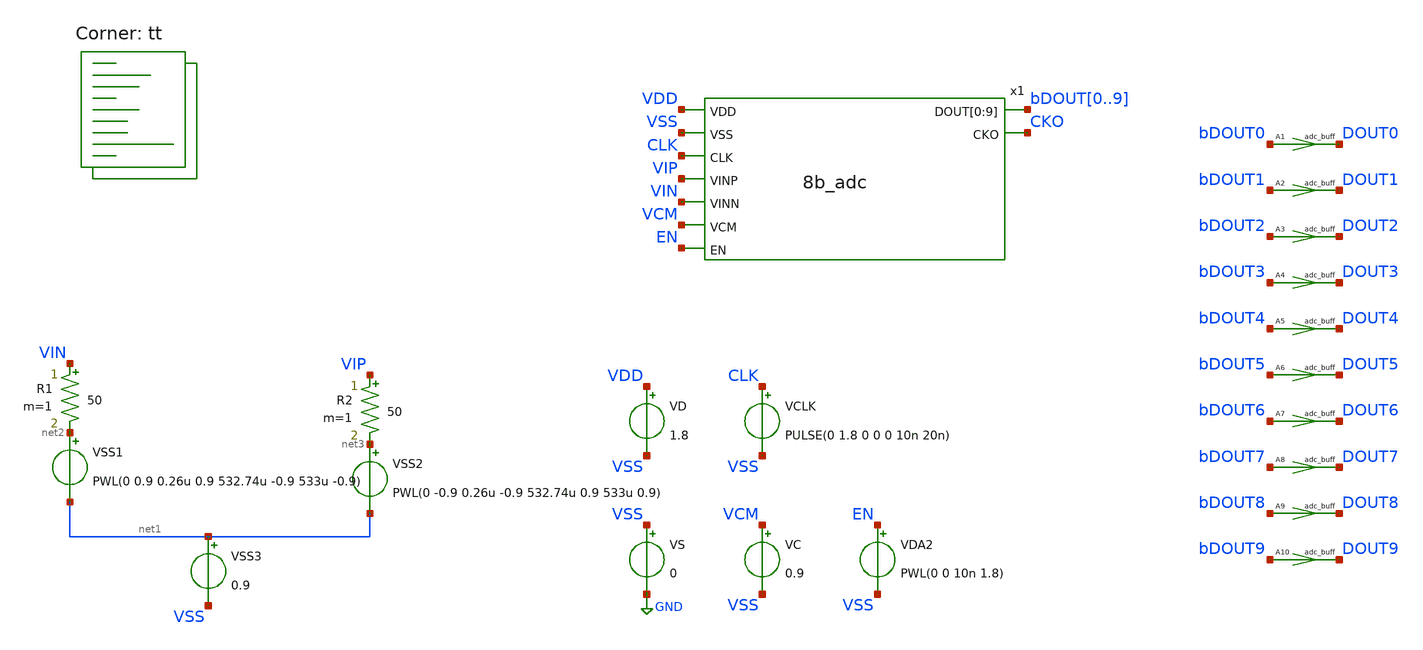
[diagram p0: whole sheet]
** sch_path: xschem/adc_tb_static.sch
**.subckt adc_tb_static
VSS1 net2 net1 PWL(0 0.9 0.26u 0.9 532.74u -0.9 533u -0.9)
VSS2 net3 net1 PWL(0 -0.9 0.26u -0.9 532.74u 0.9 533u 0.9)
VSS3 net1 VSS 0.9
R1 VIN net2 50 m=1
R2 VIP net3 50 m=1
VS VSS GND 0
VD VDD VSS 1.8
VCLK CLK VSS PULSE(0 1.8 0 0 0 10n 20n)
x1 VDD VSS CLK VIP VIN VCM EN bDOUT0 bDOUT1 bDOUT2 bDOUT3 bDOUT4 bDOUT5 bDOUT6 bDOUT7 bDOUT8 bDOUT9
+ CKO 8b_adc
VC VCM VSS 0.9
VDA2 EN VSS PWL(0 0 10n 1.8)
A1 [ bDOUT0 ] [ DOUT0 ] adc_buff
A2 [ bDOUT1 ] [ DOUT1 ] adc_buff
A3 [ bDOUT2 ] [ DOUT2 ] adc_buff
A4 [ bDOUT3 ] [ DOUT3 ] adc_buff
A5 [ bDOUT4 ] [ DOUT4 ] adc_buff
A6 [ bDOUT5 ] [ DOUT5 ] adc_buff
A7 [ bDOUT6 ] [ DOUT6 ] adc_buff
A8 [ bDOUT7 ] [ DOUT7 ] adc_buff
A9 [ bDOUT8 ] [ DOUT8 ] adc_buff
A10 [ bDOUT9 ] [ DOUT9 ] adc_buff
**** begin user architecture code

** opencircuitdesign pdks install
* .lib $::SKYWATER_MODELS/sky130.lib.spice tt
*.include $PDK_ROOT/$PDK/libs.ref/sky130_fd_sc_hdll/spice/sky130_fd_sc_hdll.spice
.include $PDK_ROOT/$PDK/libs.ref/sky130_fd_sc_hs/spice/sky130_fd_sc_hs.spice
*.include $PDK_ROOT/$PDK/libs.ref/sky130_fd_sc_hd/spice/sky130_fd_sc_hd.spice



.option wnflag=0 bypass=1
.options method=gear rawfile=binary
.options solver=klu nomod
Eout out 0 VALUE = { ((V(dout0)*512 + V(dout1)*256 + V(dout2)*128 + V(dout3)*64 + V(dout4)*32 + V(dout5)*16 + V(dout6)*8 + V(dout7)*4 + V(dout8)*2 + V(dout9)*1)/3.3) - 512 }
Epow pow 0 VALUE = { V(vdd)*(-i(vd)) }
.model adc_buff adc_bridge(in_low=0.18 in_high=1.62 rise_delay=1p fall_delay=1p)
.control
global netlist_dir .
set num_threads=32
save cko out pow vip vin
tran 1n 535u 0 1u uic; Mengubah start time menjadi 10n
rusage traniter trantime
let pow = -i(vd)*vdd
meas tran inst_pow MAX pow from=1n to=535u
meas tran avg_pow  AVG pow from=1n to=535u
remzerovec
write adc10b_tb_dynamic.raw
wrdata adc10b_tb_dynamic.txt time out cko pow
quit 1
.endc


.lib $::SKYWATER_MODELS/sky130.lib.spice tt
**** end user architecture code
**.ends
.GLOBAL GND
.end
